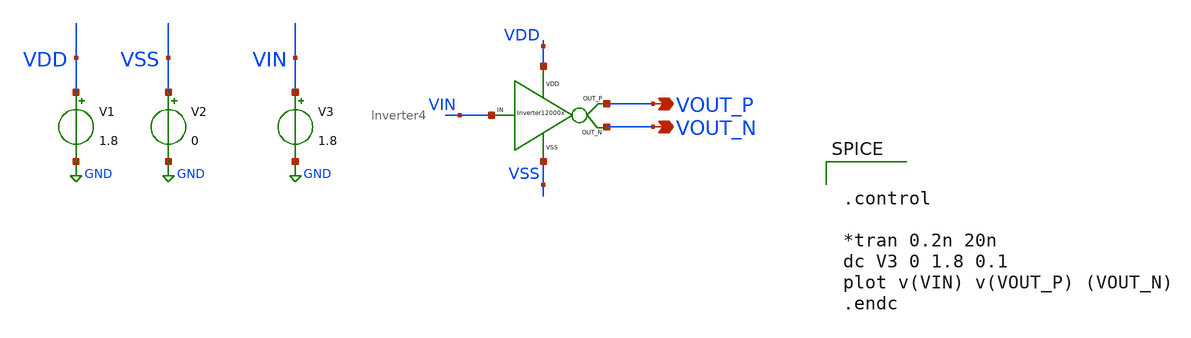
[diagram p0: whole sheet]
** sch_path: xschem/DC_DC_Converter_xschem/OTHERS/DC_DC_Converter_6/Inverter_4/Inverter4_TB.sch
**.subckt Inverter4_TB VOUT_P VOUT_N
*.opin VOUT_P
*.opin VOUT_N
V1 VDD GND 1.8
V2 VSS GND 0
V3 VIN GND 1.8
X1 VIN VOUT_P VDD VSS VOUT_N Inverter4
**** begin user architecture code


.control

*tran 0.2n 20n
dc V3 0 1.8 0.1
plot v(VIN) v(VOUT_P) (VOUT_N)
.endc



** opencircuitdesign pdks install
.lib $::SKYWATER_MODELS/sky130.lib.spice tt


**** end user architecture code
**.ends
.GLOBAL GND
.end
